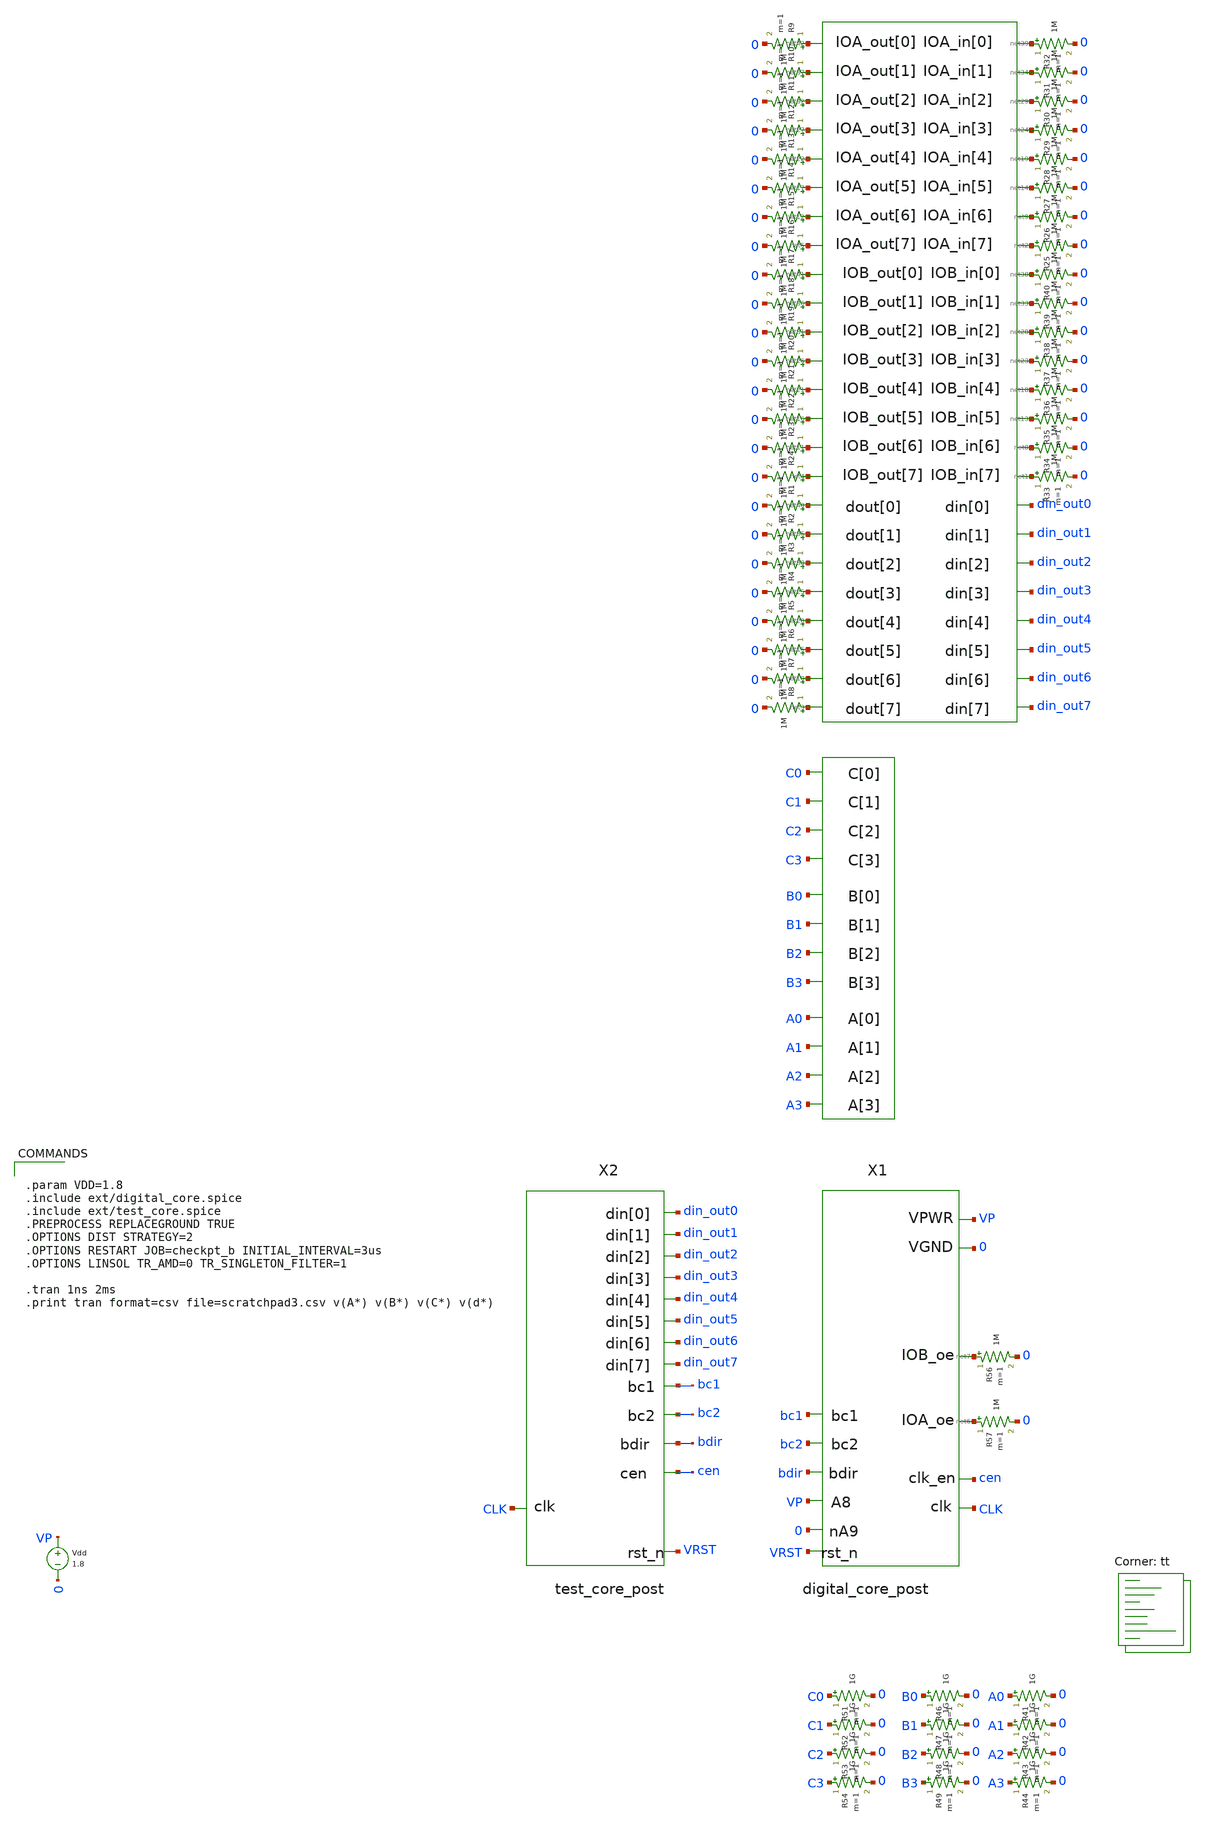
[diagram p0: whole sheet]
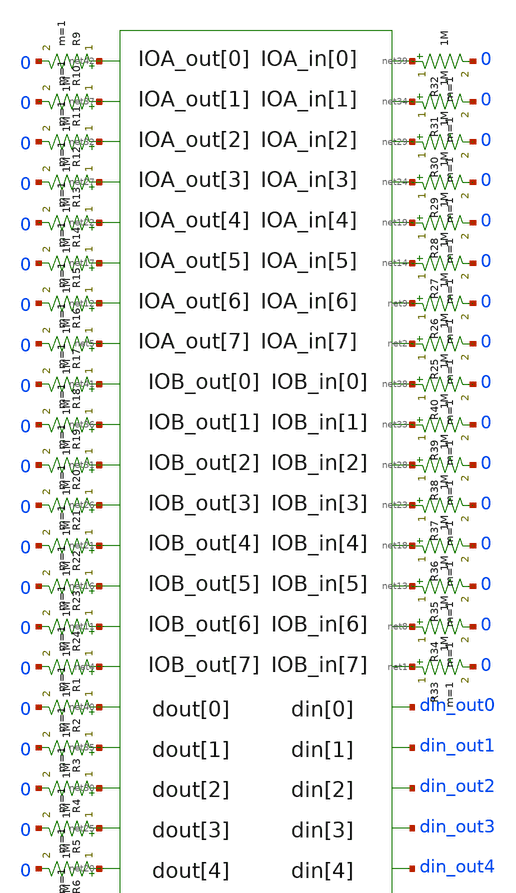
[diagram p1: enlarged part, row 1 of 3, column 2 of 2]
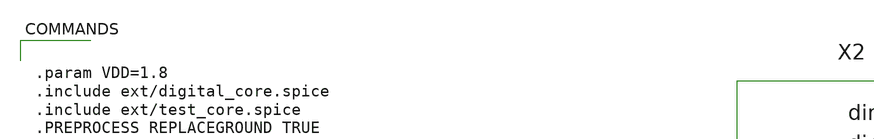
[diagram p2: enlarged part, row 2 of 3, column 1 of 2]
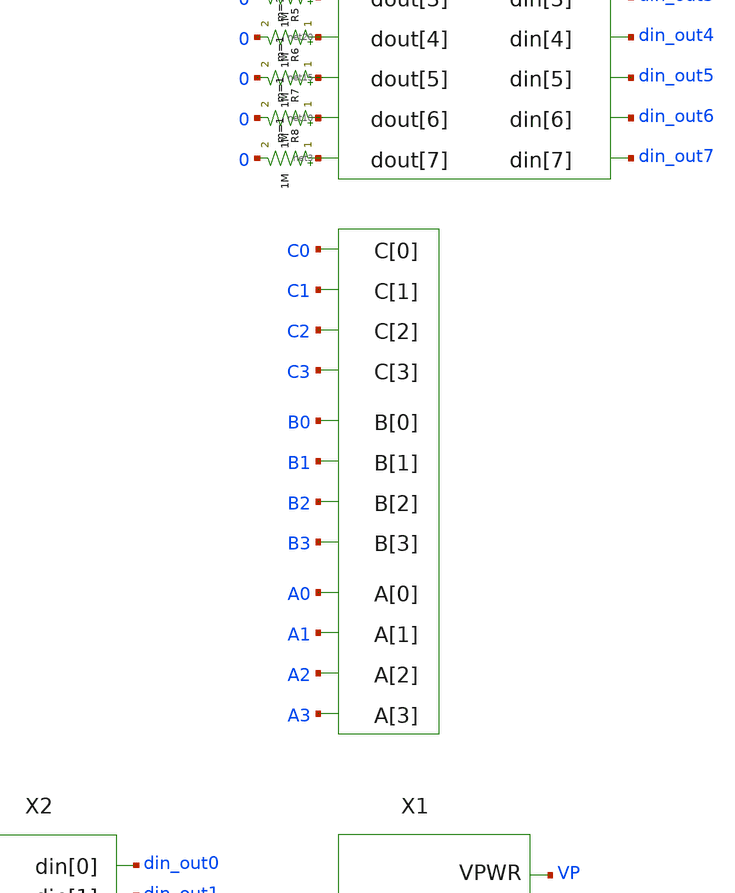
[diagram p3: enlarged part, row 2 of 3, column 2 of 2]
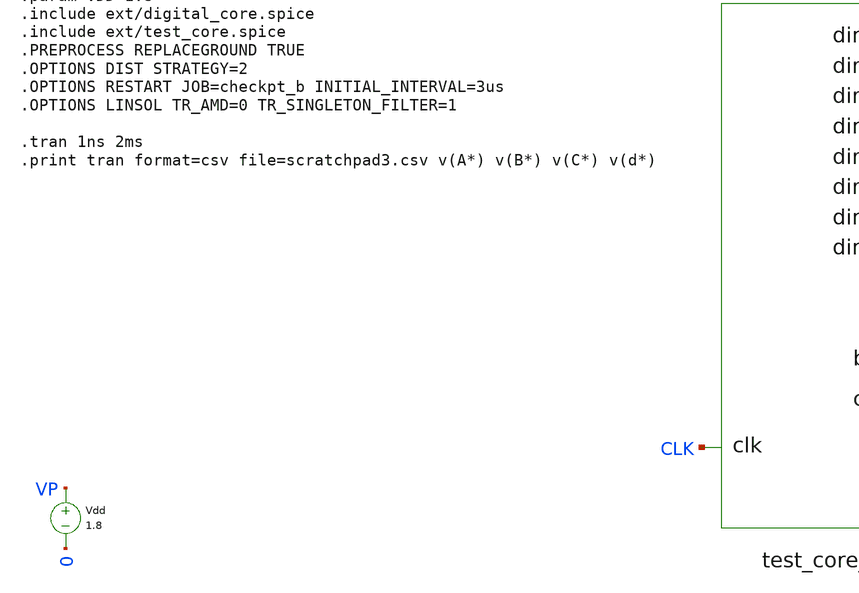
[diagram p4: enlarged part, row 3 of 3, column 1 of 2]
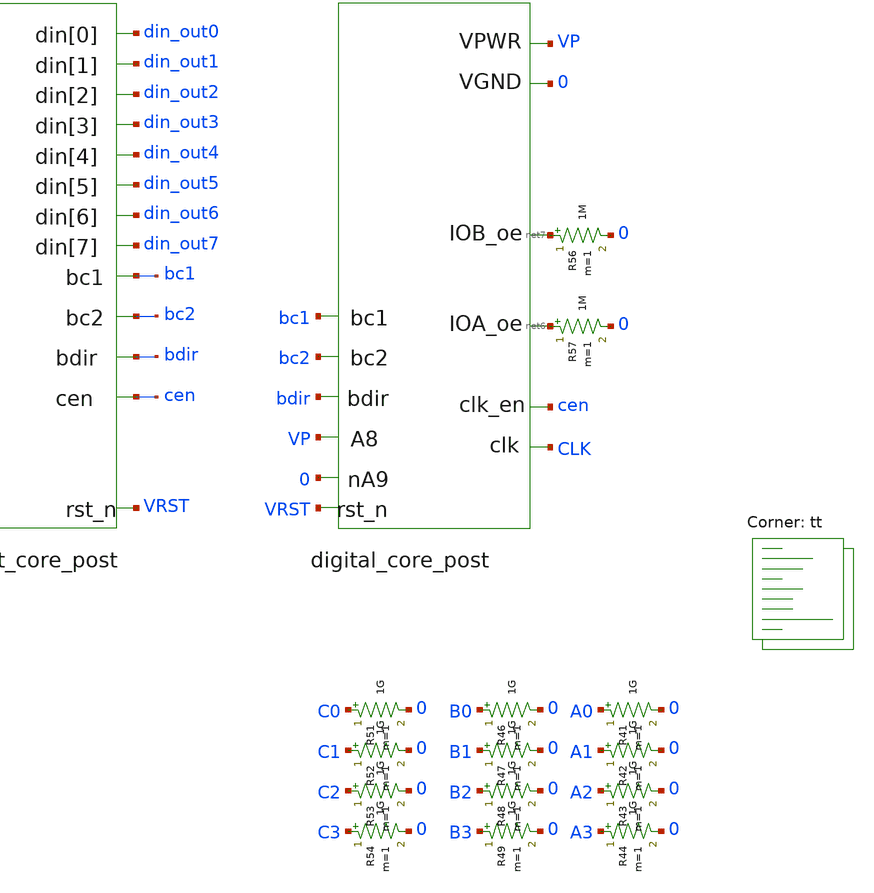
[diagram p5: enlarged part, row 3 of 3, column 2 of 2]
** sch_path: xschem/testbench_postbehavioral.sch
**.subckt testbench_postbehavioral
X1 VP A0 A1 A2 A3 B0 B1 B2 B3 C0 C1 C2 C3 net39 net34 net29 net24 net19 net14 net9 net2 net6 net42
+ net37 net32 net27 net22 net17 net12 net5 net38 net33 net28 net23 net18 net13 net8 net1 net7 net41 net36
+ net31 net26 net21 net16 net11 net4 0 VP bc1 bc2 bdir CLK cen din_out0 din_out1 din_out2 din_out3 din_out4
+ din_out5 din_out6 din_out7 net40 net35 net30 net25 net20 net15 net10 net3 0 VRST digital_core
Vdd VP 0 1.8
X2 CLK cen VRST bdir bc1 bc2 din_out7 din_out6 din_out5 din_out4 din_out3 din_out2 din_out1 din_out0
+ test_core
R1 net40 0 1M m=1
R2 net35 0 1M m=1
R3 net30 0 1M m=1
R4 net25 0 1M m=1
R5 net20 0 1M m=1
R6 net15 0 1M m=1
R7 net10 0 1M m=1
R8 net3 0 1M m=1
R9 net42 0 1M m=1
R10 net37 0 1M m=1
R11 net32 0 1M m=1
R12 net27 0 1M m=1
R13 net22 0 1M m=1
R14 net17 0 1M m=1
R15 net12 0 1M m=1
R16 net5 0 1M m=1
R17 net41 0 1M m=1
R18 net36 0 1M m=1
R19 net31 0 1M m=1
R20 net26 0 1M m=1
R21 net21 0 1M m=1
R22 net16 0 1M m=1
R23 net11 0 1M m=1
R24 net4 0 1M m=1
R25 net2 0 1M m=1
R26 net9 0 1M m=1
R27 net14 0 1M m=1
R28 net19 0 1M m=1
R29 net24 0 1M m=1
R30 net29 0 1M m=1
R31 net34 0 1M m=1
R32 net39 0 1M m=1
R33 net1 0 1M m=1
R34 net8 0 1M m=1
R35 net13 0 1M m=1
R36 net18 0 1M m=1
R37 net23 0 1M m=1
R38 net28 0 1M m=1
R39 net33 0 1M m=1
R40 net38 0 1M m=1
R56 net7 0 1M m=1
R57 net6 0 1M m=1
R41 A0 0 1G m=1
R42 A1 0 1G m=1
R43 A2 0 1G m=1
R44 A3 0 1G m=1
R46 B0 0 1G m=1
R47 B1 0 1G m=1
R48 B2 0 1G m=1
R49 B3 0 1G m=1
R51 C0 0 1G m=1
R52 C1 0 1G m=1
R53 C2 0 1G m=1
R54 C3 0 1G m=1
**** begin user architecture code


.param VDD=1.8
.include ext/digital_core.spice
.include ext/test_core.spice
.PREPROCESS REPLACEGROUND TRUE
.OPTIONS DIST STRATEGY=2
.OPTIONS RESTART JOB=checkpt_b INITIAL_INTERVAL=3us
.OPTIONS LINSOL TR_AMD=0 TR_SINGLETON_FILTER=1

.tran 1ns 2ms
.print tran format=csv file=scratchpad3.csv v(A*) v(B*) v(C*) v(d*)


.lib $::SKYWATER_MODELS/sky130.lib.spice tt
**** end user architecture code
**.ends
.end
